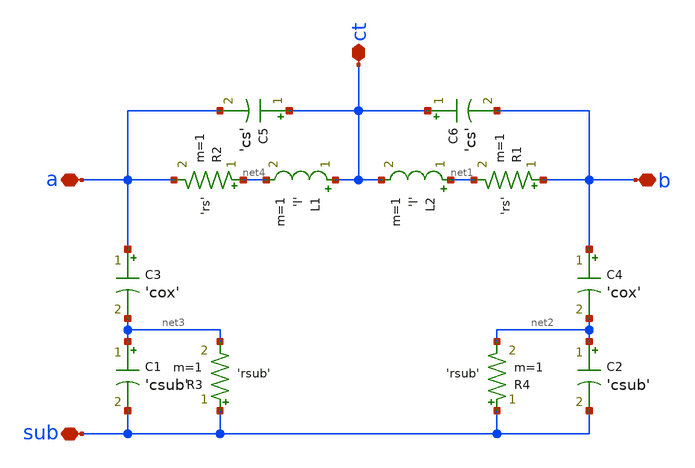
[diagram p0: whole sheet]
** sch_path: sch/inductor/inductor_spiral.sch
**.subckt inductor_spiral ct a b sub
*.iopin ct
*.iopin a
*.iopin b
*.iopin sub
C1 net3 sub 'csub' m=1
C2 net2 sub 'csub' m=1
L1 ct net4 'l' m=1
L2 net1 ct 'l' m=1
R1 b net1 'rs' m=1
R2 net4 a 'rs' m=1
R3 sub net3 'rsub' m=1
R4 sub net2 'rsub' m=1
C3 a net3 'cox' m=1
C4 b net2 'cox' m=1
C5 ct a 'cs' m=1
C6 ct b 'cs' m=1
**.ends
.end
